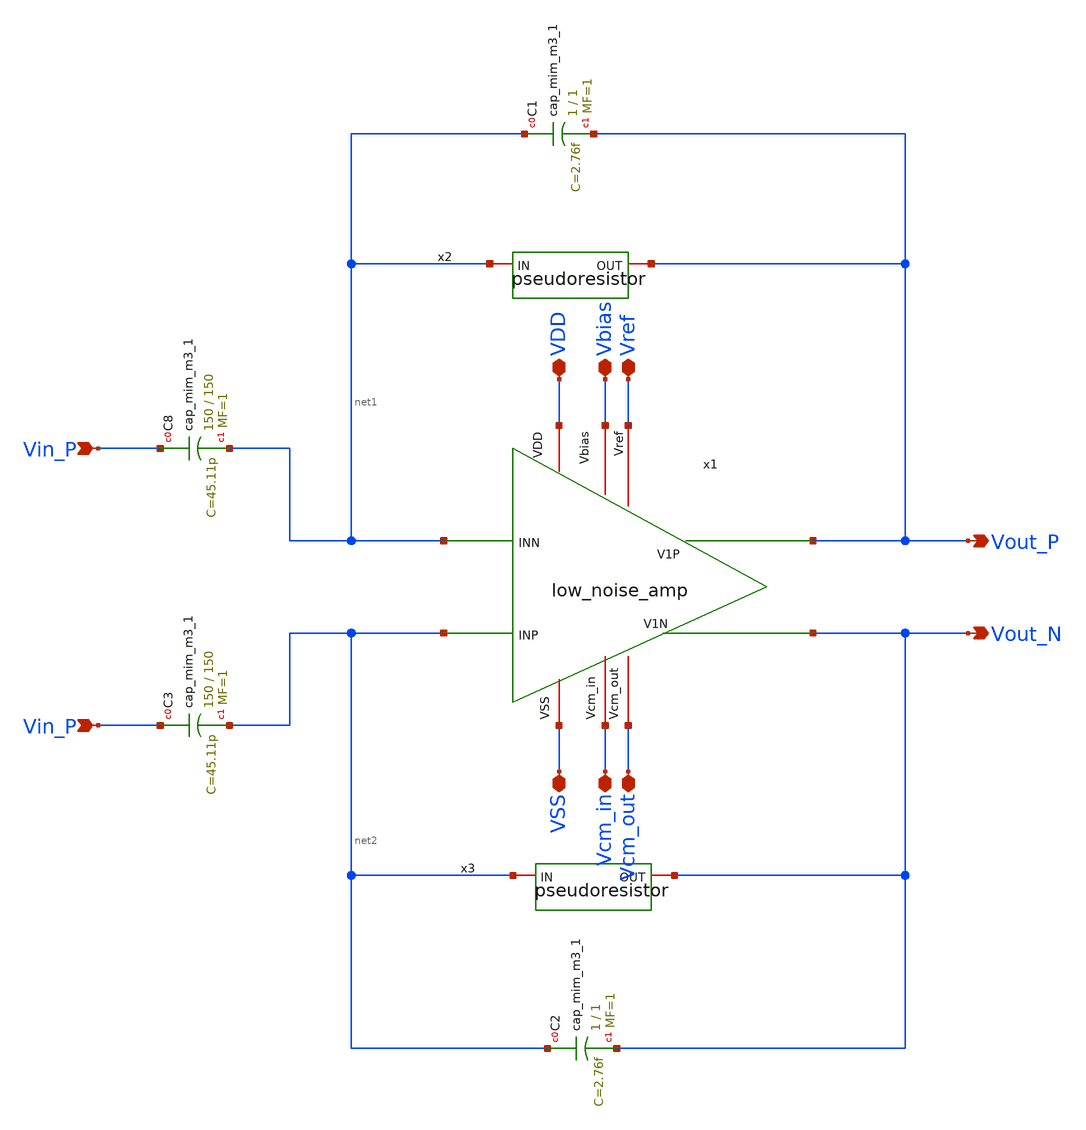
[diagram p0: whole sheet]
** sch_path: 1stage_lna.sch
**.subckt 1stage_lna VDD Vbias Vref VSS Vcm_in Vcm_out Vin_P Vin_P Vout_N Vout_P
*.iopin VDD
*.iopin Vbias
*.iopin Vref
*.iopin VSS
*.iopin Vcm_in
*.iopin Vcm_out
*.ipin Vin_P
*.ipin Vin_P
*.opin Vout_N
*.opin Vout_P
x1 VDD Vcm_in net1 net2 Vout_P Vout_N VSS Vcm_out Vbias Vref low_noise_amp
x2 net1 Vout_P pseudoresistor
XC1 net1 Vout_P sky130_fd_pr__cap_mim_m3_1 W=1 L=1 MF=1 m=1
x3 net2 Vout_N pseudoresistor
XC2 net2 Vout_N sky130_fd_pr__cap_mim_m3_1 W=1 L=1 MF=1 m=1
XC8 Vin_P net1 sky130_fd_pr__cap_mim_m3_1 W=150 L=150 MF=1 m=1
XC3 Vin_P net2 sky130_fd_pr__cap_mim_m3_1 W=150 L=150 MF=1 m=1
**.ends

* expanding   symbol:  opamp_lna/low_noise_amp.sym # of pins=10
** sym_path: opamp_lna/low_noise_amp.sym
** sch_path: opamp_lna/low_noise_amp.sch
.subckt low_noise_amp VDD Vcm_in INN INP V1P V1N VSS Vcm_out Vbias Vref
*.iopin VDD
*.iopin VSS
*.iopin Vbias
*.ipin INP
*.ipin INN
*.iopin Vref
*.iopin Vcm_in
*.iopin Vcm_out
*.opin V1N
*.opin V1P
XM3 CMFB Vref A0 VDD sky130_fd_pr__pfet_01v8 L=0.8 W=8 nf=1 ad='int((nf+1)/2) * W/nf * 0.29' as='int((nf+2)/2) * W/nf * 0.29'
+ pd='2*int((nf+1)/2) * (W/nf + 0.29)' ps='2*int((nf+2)/2) * (W/nf + 0.29)' nrd='0.29 / W' nrs='0.29 / W'
+ sa=0 sb=0 sd=0 mult=1 m=1
XM11 A0 Vbias VDD VDD sky130_fd_pr__pfet_01v8 L=0.8 W=4 nf=1 ad='int((nf+1)/2) * W/nf * 0.29' as='int((nf+2)/2) * W/nf * 0.29'
+ pd='2*int((nf+1)/2) * (W/nf + 0.29)' ps='2*int((nf+2)/2) * (W/nf + 0.29)' nrd='0.29 / W' nrs='0.29 / W'
+ sa=0 sb=0 sd=0 mult=1 m=1
XM7 V1N INP B0 VDD sky130_fd_pr__pfet_01v8 L=2 W=18 nf=1 ad='int((nf+1)/2) * W/nf * 0.29' as='int((nf+2)/2) * W/nf * 0.29'
+ pd='2*int((nf+1)/2) * (W/nf + 0.29)' ps='2*int((nf+2)/2) * (W/nf + 0.29)' nrd='0.29 / W' nrs='0.29 / W'
+ sa=0 sb=0 sd=0 mult=1 m=1
XM8 V1P INN B0 VDD sky130_fd_pr__pfet_01v8 L=2 W=18 nf=1 ad='int((nf+1)/2) * W/nf * 0.29' as='int((nf+2)/2) * W/nf * 0.29'
+ pd='2*int((nf+1)/2) * (W/nf + 0.29)' ps='2*int((nf+2)/2) * (W/nf + 0.29)' nrd='0.29 / W' nrs='0.29 / W'
+ sa=0 sb=0 sd=0 mult=1 m=1
XM9 V1N INP B1 VSS sky130_fd_pr__nfet_01v8 L=1 W=12 nf=1 ad='int((nf+1)/2) * W/nf * 0.29' as='int((nf+2)/2) * W/nf * 0.29'
+ pd='2*int((nf+1)/2) * (W/nf + 0.29)' ps='2*int((nf+2)/2) * (W/nf + 0.29)' nrd='0.29 / W' nrs='0.29 / W'
+ sa=0 sb=0 sd=0 mult=1 m=1
XM12 B0 Vbias VDD VDD sky130_fd_pr__pfet_01v8 L=0.8 W=4 nf=1 ad='int((nf+1)/2) * W/nf * 0.29' as='int((nf+2)/2) * W/nf * 0.29'
+ pd='2*int((nf+1)/2) * (W/nf + 0.29)' ps='2*int((nf+2)/2) * (W/nf + 0.29)' nrd='0.29 / W' nrs='0.29 / W'
+ sa=0 sb=0 sd=0 mult=1 m=1
XM13 B1 CMFB VSS VSS sky130_fd_pr__nfet_01v8 L=0.8 W=2 nf=1 ad='int((nf+1)/2) * W/nf * 0.29' as='int((nf+2)/2) * W/nf * 0.29'
+ pd='2*int((nf+1)/2) * (W/nf + 0.29)' ps='2*int((nf+2)/2) * (W/nf + 0.29)' nrd='0.29 / W' nrs='0.29 / W'
+ sa=0 sb=0 sd=0 mult=1 m=1
XM15 Vcm_out Vcm_out net1 Vcm_out sky130_fd_pr__pfet_01v8 L=0.6 W=1 nf=1 ad='int((nf+1)/2) * W/nf * 0.29'
+ as='int((nf+2)/2) * W/nf * 0.29' pd='2*int((nf+1)/2) * (W/nf + 0.29)' ps='2*int((nf+2)/2) * (W/nf + 0.29)'
+ nrd='0.29 / W' nrs='0.29 / W' sa=0 sb=0 sd=0 mult=5 m=5
XM16 net1 V1P V1P V1P sky130_fd_pr__pfet_01v8 L=0.6 W=1 nf=1 ad='int((nf+1)/2) * W/nf * 0.29' as='int((nf+2)/2) * W/nf * 0.29'
+ pd='2*int((nf+1)/2) * (W/nf + 0.29)' ps='2*int((nf+2)/2) * (W/nf + 0.29)' nrd='0.29 / W' nrs='0.29 / W'
+ sa=0 sb=0 sd=0 mult=5 m=5
XM17 Vcm_out Vcm_out net2 Vcm_out sky130_fd_pr__pfet_01v8 L=0.6 W=1 nf=1 ad='int((nf+1)/2) * W/nf * 0.29'
+ as='int((nf+2)/2) * W/nf * 0.29' pd='2*int((nf+1)/2) * (W/nf + 0.29)' ps='2*int((nf+2)/2) * (W/nf + 0.29)'
+ nrd='0.29 / W' nrs='0.29 / W' sa=0 sb=0 sd=0 mult=5 m=5
XM18 net2 V1N V1N V1N sky130_fd_pr__pfet_01v8 L=0.6 W=1 nf=1 ad='int((nf+1)/2) * W/nf * 0.29' as='int((nf+2)/2) * W/nf * 0.29'
+ pd='2*int((nf+1)/2) * (W/nf + 0.29)' ps='2*int((nf+2)/2) * (W/nf + 0.29)' nrd='0.29 / W' nrs='0.29 / W'
+ sa=0 sb=0 sd=0 mult=5 m=5
XC1 Vcm_out VSS sky130_fd_pr__cap_mim_m3_1 W=1 L=1 MF=1 m=1
XM1 V1P INN B1 VSS sky130_fd_pr__nfet_01v8 L=1 W=12 nf=1 ad='int((nf+1)/2) * W/nf * 0.29' as='int((nf+2)/2) * W/nf * 0.29'
+ pd='2*int((nf+1)/2) * (W/nf + 0.29)' ps='2*int((nf+2)/2) * (W/nf + 0.29)' nrd='0.29 / W' nrs='0.29 / W'
+ sa=0 sb=0 sd=0 mult=1 m=1
XM2 A1 A1 VSS VSS sky130_fd_pr__nfet_01v8 L=0.8 W=6 nf=1 ad='int((nf+1)/2) * W/nf * 0.29' as='int((nf+2)/2) * W/nf * 0.29'
+ pd='2*int((nf+1)/2) * (W/nf + 0.29)' ps='2*int((nf+2)/2) * (W/nf + 0.29)' nrd='0.29 / W' nrs='0.29 / W'
+ sa=0 sb=0 sd=0 mult=1 m=1
XM5 CMFB A1 VSS VSS sky130_fd_pr__nfet_01v8 L=0.8 W=6 nf=1 ad='int((nf+1)/2) * W/nf * 0.29' as='int((nf+2)/2) * W/nf * 0.29'
+ pd='2*int((nf+1)/2) * (W/nf + 0.29)' ps='2*int((nf+2)/2) * (W/nf + 0.29)' nrd='0.29 / W' nrs='0.29 / W'
+ sa=0 sb=0 sd=0 mult=1 m=1
XM6 A1 Vcm_in A0 VDD sky130_fd_pr__pfet_01v8 L=0.8 W=8 nf=1 ad='int((nf+1)/2) * W/nf * 0.29' as='int((nf+2)/2) * W/nf * 0.29'
+ pd='2*int((nf+1)/2) * (W/nf + 0.29)' ps='2*int((nf+2)/2) * (W/nf + 0.29)' nrd='0.29 / W' nrs='0.29 / W'
+ sa=0 sb=0 sd=0 mult=1 m=1
.ends


* expanding   symbol:  pseudoresistor.sym # of pins=2
** sym_path: pseudoresistor.sym
** sch_path: pseudoresistor.sch
.subckt pseudoresistor IN OUT
*.iopin IN
*.iopin OUT
XM5 net1 IN IN IN sky130_fd_pr__pfet_01v8 L=0.5 W=1 nf=5 ad='int((nf+1)/2) * W/nf * 0.29' as='int((nf+2)/2) * W/nf * 0.29'
+ pd='2*int((nf+1)/2) * (W/nf + 0.29)' ps='2*int((nf+2)/2) * (W/nf + 0.29)' nrd='0.29 / W' nrs='0.29 / W'
+ sa=0 sb=0 sd=0 mult=1 m=1
XM1 net2 net2 net1 net2 sky130_fd_pr__pfet_01v8 L=0.5 W=1 nf=5 ad='int((nf+1)/2) * W/nf * 0.29' as='int((nf+2)/2) * W/nf * 0.29'
+ pd='2*int((nf+1)/2) * (W/nf + 0.29)' ps='2*int((nf+2)/2) * (W/nf + 0.29)' nrd='0.29 / W' nrs='0.29 / W'
+ sa=0 sb=0 sd=0 mult=1 m=1
XM2 net3 net2 net2 net2 sky130_fd_pr__pfet_01v8 L=0.5 W=1 nf=5 ad='int((nf+1)/2) * W/nf * 0.29' as='int((nf+2)/2) * W/nf * 0.29'
+ pd='2*int((nf+1)/2) * (W/nf + 0.29)' ps='2*int((nf+2)/2) * (W/nf + 0.29)' nrd='0.29 / W' nrs='0.29 / W'
+ sa=0 sb=0 sd=0 mult=1 m=1
XM3 OUT OUT net3 OUT sky130_fd_pr__pfet_01v8 L=0.5 W=1 nf=5 ad='int((nf+1)/2) * W/nf * 0.29' as='int((nf+2)/2) * W/nf * 0.29'
+ pd='2*int((nf+1)/2) * (W/nf + 0.29)' ps='2*int((nf+2)/2) * (W/nf + 0.29)' nrd='0.29 / W' nrs='0.29 / W'
+ sa=0 sb=0 sd=0 mult=1 m=1
.ends

.end
